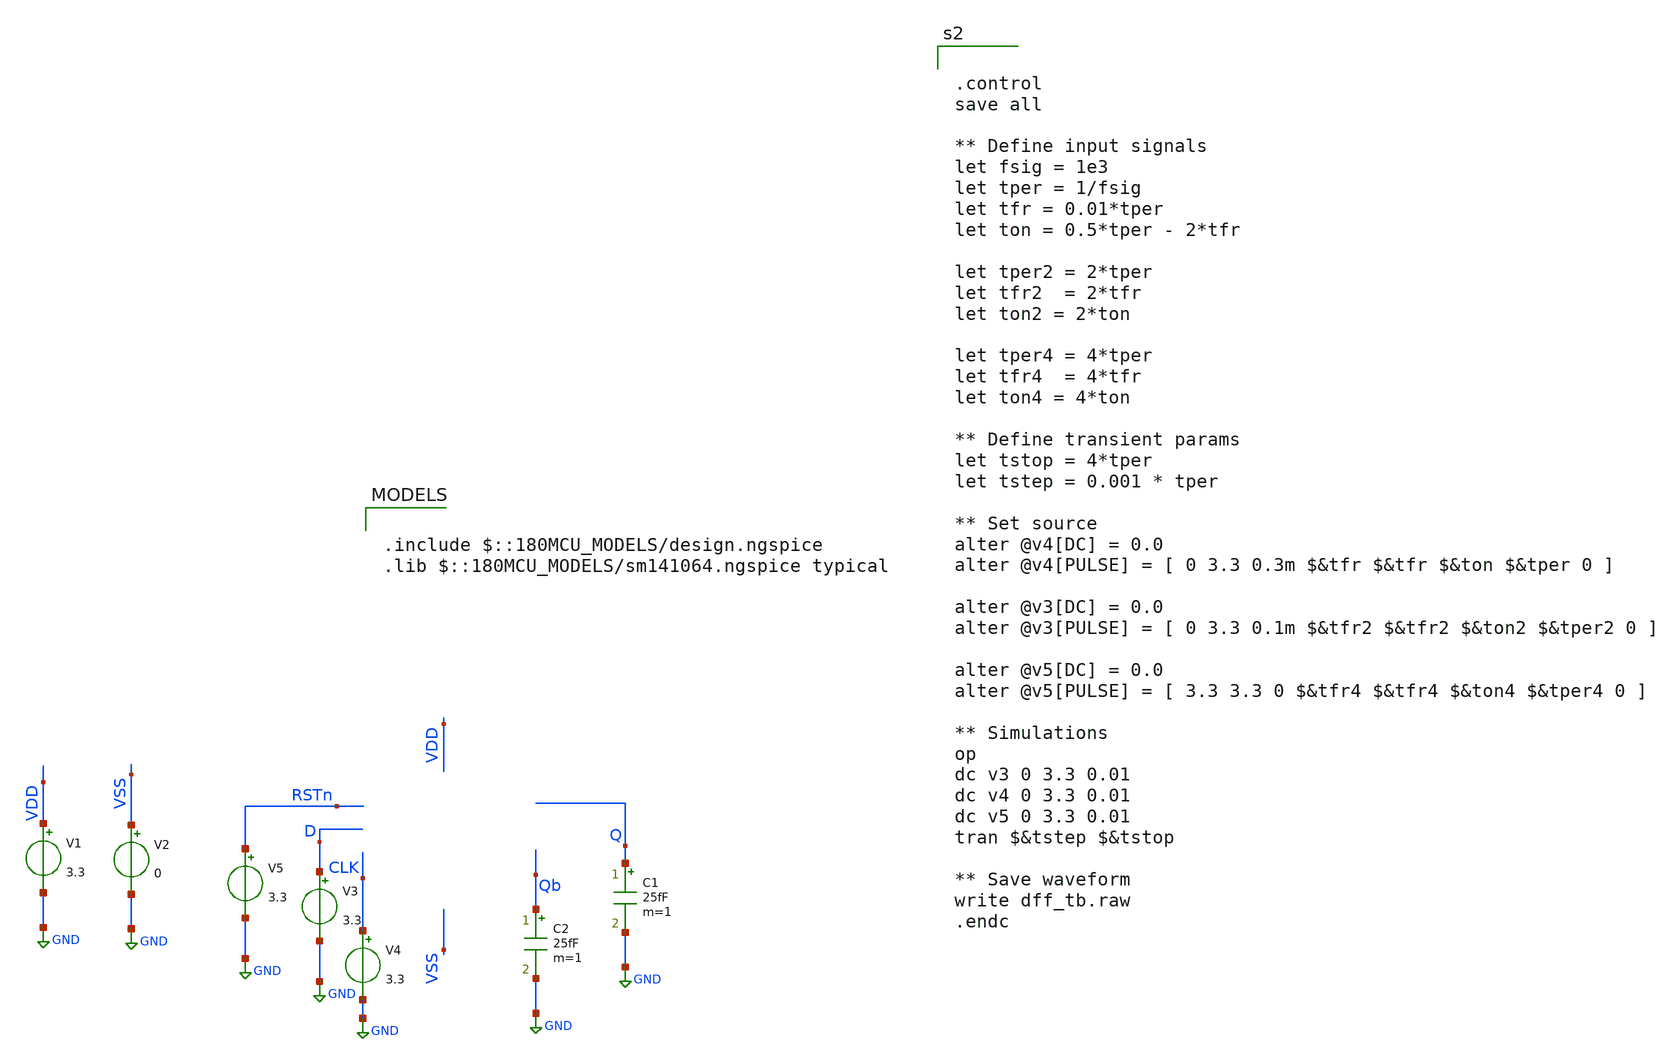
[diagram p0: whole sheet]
** sch_path: dff_postpex_tb.sch
**.subckt dff_postpex_tb
V1 VDD GND 3.3
V2 VSS GND 0
V3 D GND 3.3
C1 Q GND 25fF m=1
V4 CLK GND 3.3
C2 Qb GND 25fF m=1
V5 RSTn GND 3.3
**** begin user architecture code

.include $::180MCU_MODELS/design.ngspice
.lib $::180MCU_MODELS/sm141064.ngspice typical



.subckt dff_flat CHECK VDD CLK RSTN VSS D Q Qb
X0 a_n249_n4912# a_n1374_n6642# RSTN.t2 VSS.t12 nfet_03v3 ad=0.2646p pd=2.1u as=0.2646p ps=2.1u
+ w=0.42u l=0.28u
X1 VSS.t4 a_n359_n5759.t3 Q.t1 VSS.t3 nfet_03v3 ad=0.2646p pd=2.1u as=0.2646p ps=2.1u w=0.42u
+ l=0.28u
X2 a_n359_n5759.t1 a_n249_n4912# VDD.t23 VDD.t22 pfet_03v3 ad=0.1092p pd=0.94u as=0.2822p ps=2.18u
+ w=0.42u l=0.28u
X3 VDD.t8 a_n89_n4912# a_881_n5758# VDD.t7 pfet_03v3 ad=0.2822p pd=2.18u as=0.1092p ps=0.94u w=0.42u
+ l=0.28u
X4 VDD.t17 a_n1374_n6642# a_1067_n6116# VDD.t16 pfet_03v3 ad=0.2822p pd=2.18u as=0.1092p ps=0.94u
+ w=0.42u l=0.28u
X5 a_2281_n4424# D.t0 CHECK.t3 VSS.t19 nfet_03v3 ad=0.1092p pd=0.94u as=0.2646p ps=2.1u w=0.42u
+ l=0.28u
X6 VSS.t6 CLK.t0 a_n1342_n5730# VSS.t5 nfet_03v3 ad=0.2646p pd=2.1u as=0.2646p ps=2.1u w=0.42u
+ l=0.28u
X7 a_2280_n3998# D.t1 CHECK.t2 VDD.t4 pfet_03v3 ad=0.1092p pd=0.94u as=0.2822p ps=2.18u w=0.42u
+ l=0.28u
X8 VDD.t1 CLK.t1 a_n1342_n5730# VDD.t0 pfet_03v3 ad=0.2822p pd=2.18u as=0.2822p ps=2.18u w=0.42u
+ l=0.28u
X9 VSS.t18 a_n1342_n5730# a_n1374_n6642# VSS.t17 nfet_03v3 ad=0.2667p pd=2.11u as=0.2625p ps=2.09u
+ w=0.42u l=0.28u
X10 a_1059_n5756# RSTN.t4 a_881_n5758# VSS.t23 nfet_03v3 ad=0.1092p pd=0.94u as=0.2646p ps=2.1u
+ w=0.42u l=0.28u
X11 VSS.t1 CHECK.t4 RSTN.t0 VSS.t0 nfet_03v3 ad=0.2646p pd=2.1u as=0.2646p ps=2.1u w=0.42u l=0.28u
X12 VSS.t16 a_n1342_n5730# a_1068_n6542# VSS.t15 nfet_03v3 ad=0.2646p pd=2.1u as=0.1092p ps=0.94u
+ w=0.42u l=0.28u
X13 VSS.t25 a_n912_n3722# Qb.t1 VSS.t24 nfet_03v3 ad=0.2646p pd=2.1u as=0.2646p ps=2.1u w=0.42u
+ l=0.28u
X14 VSS.t10 a_n89_n4912# a_n181_n5757# VSS.t9 nfet_03v3 ad=0.2646p pd=2.1u as=0.1092p ps=0.94u
+ w=0.42u l=0.28u
X15 VDD.t13 a_n359_n5759.t4 Q.t0 VDD.t12 pfet_03v3 ad=0.2822p pd=2.18u as=0.2822p ps=2.18u w=0.42u
+ l=0.28u
X16 a_n249_n4912# a_n1342_n5730# RSTN.t3 VDD.t21 pfet_03v3 ad=0.2822p pd=2.18u as=0.2822p ps=2.18u
+ w=0.42u l=0.28u
X17 VSS.t22 a_n359_n5759.t5 a_n912_n3722# VSS.t21 nfet_03v3 ad=0.2646p pd=2.1u as=0.2646p ps=2.1u
+ w=0.42u l=0.28u
X18 VDD.t20 a_n1342_n5730# a_n1374_n6642# VDD.t19 pfet_03v3 ad=0.2822p pd=2.18u as=0.2822p ps=2.18u
+ w=0.42u l=0.28u
X19 a_881_n5758# a_n1374_n6642# CHECK.t0 VSS.t11 nfet_03v3 ad=0.2646p pd=2.1u as=0.2646p ps=2.1u
+ w=0.42u l=0.28u
X20 VDD.t27 a_n912_n3722# Qb.t0 VDD.t26 pfet_03v3 ad=0.2822p pd=2.18u as=0.2822p ps=2.18u w=0.42u
+ l=0.28u
X21 VSS.t14 a_n1342_n5730# a_2281_n4424# VSS.t13 nfet_03v3 ad=0.2646p pd=2.1u as=0.1092p ps=0.94u
+ w=0.42u l=0.28u
X22 VDD.t6 a_n89_n4912# a_n359_n5759.t0 VDD.t5 pfet_03v3 ad=0.2822p pd=2.18u as=0.1092p ps=0.94u
+ w=0.42u l=0.28u
X23 VDD.t15 a_n1374_n6642# a_2280_n3998# VDD.t14 pfet_03v3 ad=0.2822p pd=2.18u as=0.1092p ps=0.94u
+ w=0.42u l=0.28u
X24 a_1067_n6116# a_n359_n5759.t6 a_n249_n4912# VDD.t11 pfet_03v3 ad=0.1092p pd=0.94u as=0.2822p
+ ps=2.18u w=0.42u l=0.28u
X25 a_881_n5758# RSTN.t5 VDD.t25 VDD.t24 pfet_03v3 ad=0.1092p pd=0.94u as=0.2822p ps=2.18u w=0.42u
+ l=0.28u
X26 VSS.t8 a_n89_n4912# a_1059_n5756# VSS.t7 nfet_03v3 ad=0.2646p pd=2.1u as=0.1092p ps=0.94u
+ w=0.42u l=0.28u
X27 VDD.t3 CHECK.t5 RSTN.t1 VDD.t2 pfet_03v3 ad=0.2822p pd=2.18u as=0.2822p ps=2.18u w=0.42u l=0.28u
X28 a_881_n5758# a_n1342_n5730# CHECK.t1 VDD.t18 pfet_03v3 ad=0.2822p pd=2.18u as=0.2822p ps=2.18u
+ w=0.42u l=0.28u
X29 a_1068_n6542# a_n359_n5759.t7 a_n249_n4912# VSS.t2 nfet_03v3 ad=0.1092p pd=0.94u as=0.2646p
+ ps=2.1u w=0.42u l=0.28u
X30 a_n181_n5757# a_n249_n4912# a_n359_n5759.t2 VSS.t20 nfet_03v3 ad=0.1092p pd=0.94u as=0.2646p
+ ps=2.1u w=0.42u l=0.28u
X31 VDD.t10 a_n359_n5759.t8 a_n912_n3722# VDD.t9 pfet_03v3 ad=0.2822p pd=2.18u as=0.2822p ps=2.18u
+ w=0.42u l=0.28u
R0 RSTN.t5 RSTN.n3 72.3487
R1 RSTN RSTN.t5 24.9493
R2 RSTN.n3 RSTN.t4 16.9469
R3 RSTN.n1 RSTN.t2 12.9962
R4 RSTN.n0 RSTN.t1 12.66
R5 RSTN.n0 RSTN.t0 12.3135
R6 RSTN.n1 RSTN.t3 12.0263
R7 RSTN.n3 RSTN.n2 9.90023
R8 RSTN.n2 RSTN.n1 0.39464
R9 RSTN.n2 RSTN.n0 0.156576
R10 VSS.n23 VSS.n16 749278
R11 VSS.n16 VSS.t19 91327.6
R12 VSS.n5 VSS.n3 64653.5
R13 VSS.n50 VSS.n3 47027.8
R14 VSS.n13 VSS.n8 11150.5
R15 VSS.t24 VSS.n46 10656.3
R16 VSS.n46 VSS.n45 9310.54
R17 VSS.n6 VSS.n3 9172.39
R18 VSS.n17 VSS.n8 8859.18
R19 VSS.n46 VSS.n7 7710.44
R20 VSS.n43 VSS.n9 6769.51
R21 VSS.n35 VSS.n34 6625.47
R22 VSS.n45 VSS.n8 5874.35
R23 VSS.t17 VSS.n49 4464.13
R24 VSS.n13 VSS.n11 4354.26
R25 VSS.n30 VSS.n10 4226.8
R26 VSS.n29 VSS.n11 4102.23
R27 VSS.n45 VSS.n44 3676.98
R28 VSS.n24 VSS.n23 3564.92
R29 VSS.n44 VSS.t11 2894.81
R30 VSS.n47 VSS.n7 2588.74
R31 VSS.t3 VSS.n3 2474.65
R32 VSS.n49 VSS.n48 2224.45
R33 VSS.n49 VSS.t5 1774.36
R34 VSS.n48 VSS.n6 1755.92
R35 VSS.n22 VSS.n21 1702.15
R36 VSS.t0 VSS.n24 1689.9
R37 VSS.n24 VSS.n10 1589.78
R38 VSS.t5 VSS.n5 1493.57
R39 VSS.t13 VSS.n15 1430.46
R40 VSS.n25 VSS.t0 1413.04
R41 VSS.t23 VSS.n9 1360.03
R42 VSS.n21 VSS.t11 1205.49
R43 VSS.t21 VSS.n7 1196.19
R44 VSS.n48 VSS.n47 1177.13
R45 VSS.n18 VSS.t7 1172.44
R46 VSS.n23 VSS.n22 1095.11
R47 VSS.n25 VSS.n11 1090.87
R48 VSS.n36 VSS.t9 1070.49
R49 VSS.n34 VSS.t2 1055.67
R50 VSS.n42 VSS.t21 992.063
R51 VSS.n30 VSS.t12 940.115
R52 VSS.n50 VSS.t17 920.712
R53 VSS.t19 VSS.t13 915.494
R54 VSS.n18 VSS.n10 900.433
R55 VSS.n34 VSS.n33 836.077
R56 VSS.n36 VSS.n35 822.135
R57 VSS.n32 VSS.n30 797.649
R58 VSS.t7 VSS.t23 750.361
R59 VSS.t9 VSS.t20 685.112
R60 VSS.n17 VSS.n16 674.74
R61 VSS.n38 VSS.n7 671.655
R62 VSS.n43 VSS.n42 615.08
R63 VSS.n33 VSS.t3 604.99
R64 VSS.t15 VSS.n32 576.241
R65 VSS.t12 VSS.n29 492.724
R66 VSS.n44 VSS.n43 472.2
R67 VSS.n15 VSS.n13 469.19
R68 VSS.t20 VSS.n6 466.733
R69 VSS.n47 VSS.t24 415.238
R70 VSS.t2 VSS.t15 368.795
R71 VSS.n35 VSS.n9 317.529
R72 VSS.n22 VSS.n17 57.864
R73 VSS.n21 VSS.n20 15.3475
R74 VSS.n51 VSS.t18 12.5437
R75 VSS.n37 VSS.t10 12.4687
R76 VSS.n31 VSS.t16 12.4687
R77 VSS.n19 VSS.t8 12.4687
R78 VSS.n26 VSS.t1 12.4687
R79 VSS.n41 VSS.t22 12.4687
R80 VSS.n4 VSS.t6 12.4687
R81 VSS.n1 VSS.t4 12.4687
R82 VSS.n38 VSS.t25 12.4687
R83 VSS.n14 VSS.t14 12.4675
R84 VSS.n29 VSS.n28 11.6695
R85 VSS.n15 VSS.n14 10.4017
R86 VSS.n19 VSS.n18 10.4005
R87 VSS.n26 VSS.n25 10.4005
R88 VSS.n5 VSS.n4 10.4005
R89 VSS.n33 VSS.n1 10.4005
R90 VSS.n51 VSS.n50 10.4005
R91 VSS.n42 VSS.n41 10.4005
R92 VSS.n32 VSS.n31 10.4005
R93 VSS.n37 VSS.n36 10.4005
R94 VSS.n31 VSS.n0 9.86036
R95 VSS.n28 VSS.n27 6.42418
R96 VSS.n20 VSS.n19 6.02652
R97 VSS.n39 VSS.n38 5.75457
R98 VSS.n39 VSS.n2 5.48837
R99 VSS.n41 VSS.n40 5.44665
R100 VSS.n40 VSS.n37 5.3877
R101 VSS.n27 VSS.n26 4.66984
R102 VSS.n14 VSS.n12 4.6547
R103 VSS.n20 VSS.n12 1.34731
R104 VSS.n40 VSS.n39 1.2245
R105 VSS.n27 VSS.n12 1.03428
R106 VSS.n52 VSS.n2 0.820259
R107 VSS VSS.n0 0.783577
R108 VSS.n28 VSS.n0 0.664346
R109 VSS.n53 VSS.n52 0.652808
R110 VSS VSS.n53 0.348192
R111 VSS.n4 VSS.n2 0.323682
R112 VSS.n53 VSS.n1 0.322765
R113 VSS.n52 VSS.n51 0.314599
R114 a_n359_n5759.t8 a_n359_n5759.t5 69.3505
R115 a_n359_n5759.t4 a_n359_n5759.t3 69.3505
R116 a_n359_n5759.t6 a_n359_n5759.t7 53.4469
R117 a_n359_n5759.n0 a_n359_n5759.t6 35.2609
R118 a_n359_n5759.n2 a_n359_n5759.t8 30.3133
R119 a_n359_n5759.n0 a_n359_n5759.t4 25.048
R120 a_n359_n5759.n1 a_n359_n5759.t2 12.3005
R121 a_n359_n5759.n3 a_n359_n5759.n2 5.78668
R122 a_n359_n5759.t0 a_n359_n5759.n3 4.33383
R123 a_n359_n5759.n3 a_n359_n5759.t1 4.33383
R124 a_n359_n5759.n1 a_n359_n5759.n0 0.519935
R125 a_n359_n5759.n2 a_n359_n5759.n1 0.494983
R126 Q Q.t1 12.6202
R127 Q Q.t0 12.341
R128 VDD.n8 VDD.t21 715.11
R129 VDD.n11 VDD.t18 714.49
R130 VDD.n18 VDD.t19 713.694
R131 VDD.n14 VDD.t26 713.688
R132 VDD.n17 VDD.t0 713.688
R133 VDD.n12 VDD.t5 713.688
R134 VDD.n16 VDD.t9 713.688
R135 VDD.n9 VDD.t14 713.688
R136 VDD.n6 VDD.t2 713.688
R137 VDD.n0 VDD.t7 713.688
R138 VDD.n3 VDD.t16 713.688
R139 VDD.n2 VDD.t12 713.688
R140 VDD.t5 VDD.t22 434.784
R141 VDD.t14 VDD.t4 434.784
R142 VDD.t7 VDD.t24 434.784
R143 VDD.t16 VDD.t11 434.784
R144 VDD.n0 VDD.t25 13.7623
R145 VDD.n13 VDD.t23 12.5331
R146 VDD.n17 VDD.t1 12.1992
R147 VDD.n16 VDD.t10 12.1992
R148 VDD.n6 VDD.t3 12.1992
R149 VDD.n3 VDD.t17 12.1992
R150 VDD.n2 VDD.t13 12.1992
R151 VDD.n14 VDD.t27 12.198
R152 VDD.n10 VDD.t15 12.1968
R153 VDD.n18 VDD.t20 12.192
R154 VDD.n12 VDD.t6 12.1422
R155 VDD.n1 VDD.t8 12.1411
R156 VDD.n19 VDD.n18 11.4596
R157 VDD.n16 VDD.n15 9.90617
R158 VDD.n4 VDD.n2 7.0573
R159 VDD.n7 VDD.n5 5.46986
R160 VDD.n5 VDD.n1 5.05424
R161 VDD.n4 VDD.n3 5.0066
R162 VDD.n20 VDD.n19 3.429
R163 VDD.n11 VDD.n10 1.6793
R164 VDD.n19 VDD.n17 1.5236
R165 VDD.n9 VDD.n8 1.27962
R166 VDD.n13 VDD.n12 1.1387
R167 VDD VDD.n11 0.864995
R168 VDD.n5 VDD.n4 0.845079
R169 VDD.n20 VDD.n16 0.527474
R170 VDD.n15 VDD.n14 0.516611
R171 VDD.n15 VDD.n13 0.457423
R172 VDD.n8 VDD.n7 0.351026
R173 VDD VDD.n20 0.00545413
R174 VDD.n10 VDD.n9 0.00286842
R175 VDD.n7 VDD.n6 0.00168421
R176 VDD.n1 VDD.n0 0.00153448
R177 D.t1 D.t0 53.4469
R178 D D.t1 24.9505
R179 CHECK.t5 CHECK.t4 69.3505
R180 CHECK.n1 CHECK.t5 25.414
R181 CHECK.n0 CHECK.t1 12.667
R182 CHECK CHECK.t2 12.3758
R183 CHECK.n2 CHECK.t3 12.3005
R184 CHECK.n0 CHECK.t0 12.3005
R185 CHECK.n1 CHECK.n0 1.9362
R186 CHECK.n2 CHECK.n1 0.19099
R187 CHECK CHECK.n2 0.179078
R188 CLK.t1 CLK.t0 69.3505
R189 CLK CLK.t1 24.9517
R190 Qb Qb.t1 12.6395
R191 Qb Qb.t0 12.3217
C0 RSTN CHECK 0.10365f
C1 VDD a_n89_n4912# 0.80322f
C2 a_n1342_n5730# a_881_n5758# 0.31376f
C3 a_n249_n4912# VDD 0.56511f
C4 a_n1374_n6642# a_n249_n4912# 0.23084f
C5 RSTN VDD 0.76938f
C6 a_n249_n4912# a_n89_n4912# 0.28644f
C7 a_881_n5758# CHECK 0.25267f
C8 RSTN a_n1374_n6642# 0.22275f
C9 RSTN a_n89_n4912# 0.29193f
C10 VDD a_n1342_n5730# 1.71536f
C11 RSTN a_n249_n4912# 0.11019f
C12 a_n1374_n6642# a_n1342_n5730# 1.67868f
C13 VDD a_881_n5758# 1.18904f
C14 CLK VDD 0.28794f
C15 a_n1374_n6642# a_881_n5758# 0.24946f
C16 VDD CHECK 0.95856f
C17 a_n249_n4912# a_n1342_n5730# 0.21283f
C18 a_n1374_n6642# CHECK 0.2678f
C19 a_n912_n3722# VDD 0.83176f
C20 a_n249_n4912# a_881_n5758# 0.19693f
C21 Qb VDD 0.10704f
C22 RSTN a_881_n5758# 0.35092f
C23 a_n1374_n6642# VDD 1.886f
C24 VDD D 0.18707f
C25 Q VSS 0.25589f
C26 CLK VSS 0.39888f
C27 RSTN VSS 1.33038f
C28 CHECK VSS 1.26966f
C29 D VSS 0.27844f
C30 Qb VSS 0.15428f
C31 VDD VSS 18.83505f
C32 a_n89_n4912# VSS 1.32962f
C33 a_n249_n4912# VSS 2.53842f
C34 a_881_n5758# VSS 0.89126f
C35 a_n1374_n6642# VSS 5.44569f
C36 a_n1342_n5730# VSS 6.88765f
C37 a_n912_n3722# VSS 0.62392f
C38 VDD.n8 VSS 0.11133f
C39 VDD.n11 VSS 0.13113f
C40 VDD.n19 VSS 0.21025f
C41 VDD.n20 VSS 0.10843f
C42 a_n359_n5759.t8 VSS 0.19196f
C43 a_n359_n5759.t6 VSS 0.11284f
C44 a_n359_n5759.n0 VSS 0.45569f
C45 a_n359_n5759.n1 VSS 0.14466f
C46 a_n359_n5759.n2 VSS 1.35777f
.ends
X0 CHECK VDD CLK RSTN VSS D Q Qb dff_flat




.control
save all

** Define input signals
let fsig = 1e3
let tper = 1/fsig
let tfr = 0.01*tper
let ton = 0.5*tper - 2*tfr

let tper2 = 2*tper
let tfr2  = 2*tfr
let ton2 = 2*ton

let tper4 = 4*tper
let tfr4  = 4*tfr
let ton4 = 4*ton

** Define transient params
let tstop = 4*tper
let tstep = 0.001 * tper

** Set source
alter @v4[DC] = 0.0
alter @v4[PULSE] = [ 0 3.3 0.3m $&tfr $&tfr $&ton $&tper 0 ]

alter @v3[DC] = 0.0
alter @v3[PULSE] = [ 0 3.3 0.1m $&tfr2 $&tfr2 $&ton2 $&tper2 0 ]

alter @v5[DC] = 0.0
alter @v5[PULSE] = [ 3.3 3.3 0 $&tfr4 $&tfr4 $&ton4 $&tper4 0 ]

** Simulations
op
dc v3 0 3.3 0.01
dc v4 0 3.3 0.01
dc v5 0 3.3 0.01
tran $&tstep $&tstop

** Save waveform
write dff_tb.raw
.endc


**** end user architecture code
**.ends
.GLOBAL GND
.end
